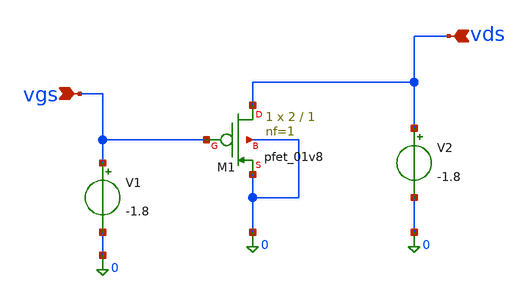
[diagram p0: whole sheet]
** sch_path: pmosvi.sch
**.subckt pmosvi vgs vds
*.ipin vgs
*.ipin vds
XM1 vds vgs 0 0 sky130_fd_pr__pfet_01v8 L=1 W=2 nf=1 ad='int((1 + 1)/2) * 2 / 1 * 0.29' as='int((1 + 2)/2) * 2 / 1 * 0.29'
+ pd='2*int((1 + 1)/2) * (2 / 1 + 0.29)' ps='2*int((1 + 2)/2) * (2 / 1 + 0.29)' nrd='0.29 / 2 ' nrs='0.29 / 2 '
+ sa=0 sb=0 sd=0 mult=1 m=1
V1 vgs 0 -1.8
V2 vds 0 -1.8
**** begin user architecture code


.lib /foss/pdks/ciel/sky130/versions/7b70722e33c03fcb5dabcf4d479fb0822d9251c9/sky130A/libs.tech/ngspice/sky130.lib.spice tt
.control
  save all
  save @m.xm1.msky130_fd_pr__pfet_01v8[id]
  save @m.xm1.msky130_fd_pr__pfet_01v8[gm]

  op

  * --- Output Characteristics (Id-Vds) ---
  dc v2 0 -1.8 -0.1 v1 0 -1.8 -0.2
  * Negating the current to force the standard negative plot
  plot -@m.xm1.msky130_fd_pr__pfet_01v8[id]
  plot @m.xm1.msky130_fd_pr__pfet_01v8[gm]

  * --- Transfer Characteristics (Id-Vgs) ---
  dc v1 0 -1.8 -0.1
  * Negating the current here as well
  plot -@m.xm1.msky130_fd_pr__pfet_01v8[id]
  plot @m.xm1.msky130_fd_pr__pfet_01v8[gm]

  print @m.xm1.msky130_fd_pr__pfet_01v8[id]
  print @m.xm1.msky130_fd_pr__pfet_01v8[gm]
  print @m.xm1.msky130_fd_pr__pfet_01v8[vth]
  print @m.xm1.msky130_fd_pr__pfet_01v8[vgs]
  print @m.xm1.msky130_fd_pr__pfet_01v8[vdsat]
  print @m.xm1.msky130_fd_pr__pfet_01v8[vds]
  print @m.xm1.msky130_fd_pr__pfet_01v8[gds]

  write pmosvi.raw
.endc


**** end user architecture code
**.ends
.end
